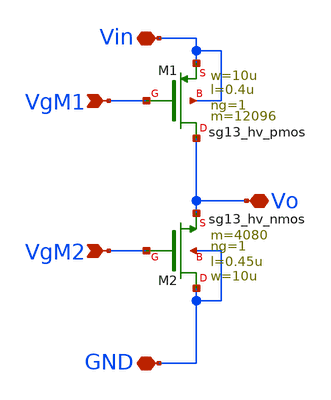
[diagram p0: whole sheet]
** sch_path: ChipUSM_AnalogTrack24/DCDCBuck/DCDCBuck_vto1p1.sch
**.subckt DCDCBuck_vto1p1 Vin VgM1 VgM2 Vo GND
*.iopin Vin
*.ipin VgM1
*.ipin VgM2
*.iopin Vo
*.iopin GND
XM2 GND VgM2 Vo GND sg13_hv_nmos w=10u l=0.45u ng=1 m=4080 mm_ok=1
XM1 Vo VgM1 Vin Vin sg13_hv_pmos w=10u l=0.4u ng=1 m=12096 mm_ok=1
**.ends
.end
